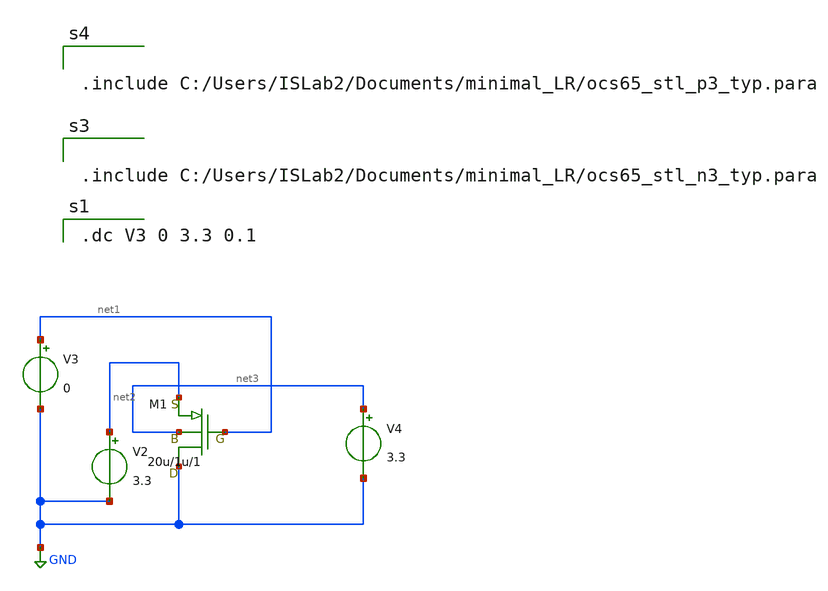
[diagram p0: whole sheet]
** sch_path: idvg.sch
**.subckt idvg
M1 GND net1 net2 net3 pch w=20u l=1u as=0 ps=0 ad=0 pd=0 m=1
V2 net2 GND 3.3
V3 net1 GND 0
V4 net3 GND 3.3
**** begin user architecture code

.dc V3 0 3.3 0.1



.include C:/Users/ISLab2/Documents/minimal_LR/ocs65_stl_n3_typ.para



.include C:/Users/ISLab2/Documents/minimal_LR/ocs65_stl_p3_typ.para

**** end user architecture code
**.ends
.GLOBAL GND
.end
